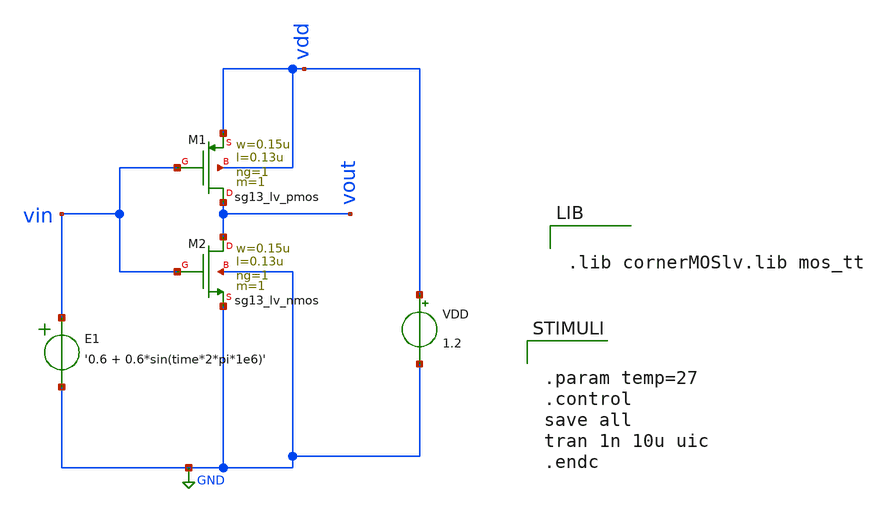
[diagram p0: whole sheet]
** sch_path: lab2-3.sch
**.subckt lab2-3
XM2 vout vin GND GND sg13_lv_nmos w=0.15u l=0.13u ng=1 m=1 mm_ok=1
VDD vdd GND 1.2
XM1 vout vin vdd vdd sg13_lv_pmos w=0.15u l=0.13u ng=1 m=1 mm_ok=1
E1 vin GND VOL=' '0.6 + 0.6*sin(time*2*pi*1e6)' '
**** begin user architecture code


.lib cornerMOSlv.lib mos_tt



.param temp=27
.control
save all
tran 1n 10u uic
.endc


**** end user architecture code
**.ends
.GLOBAL GND
.end
